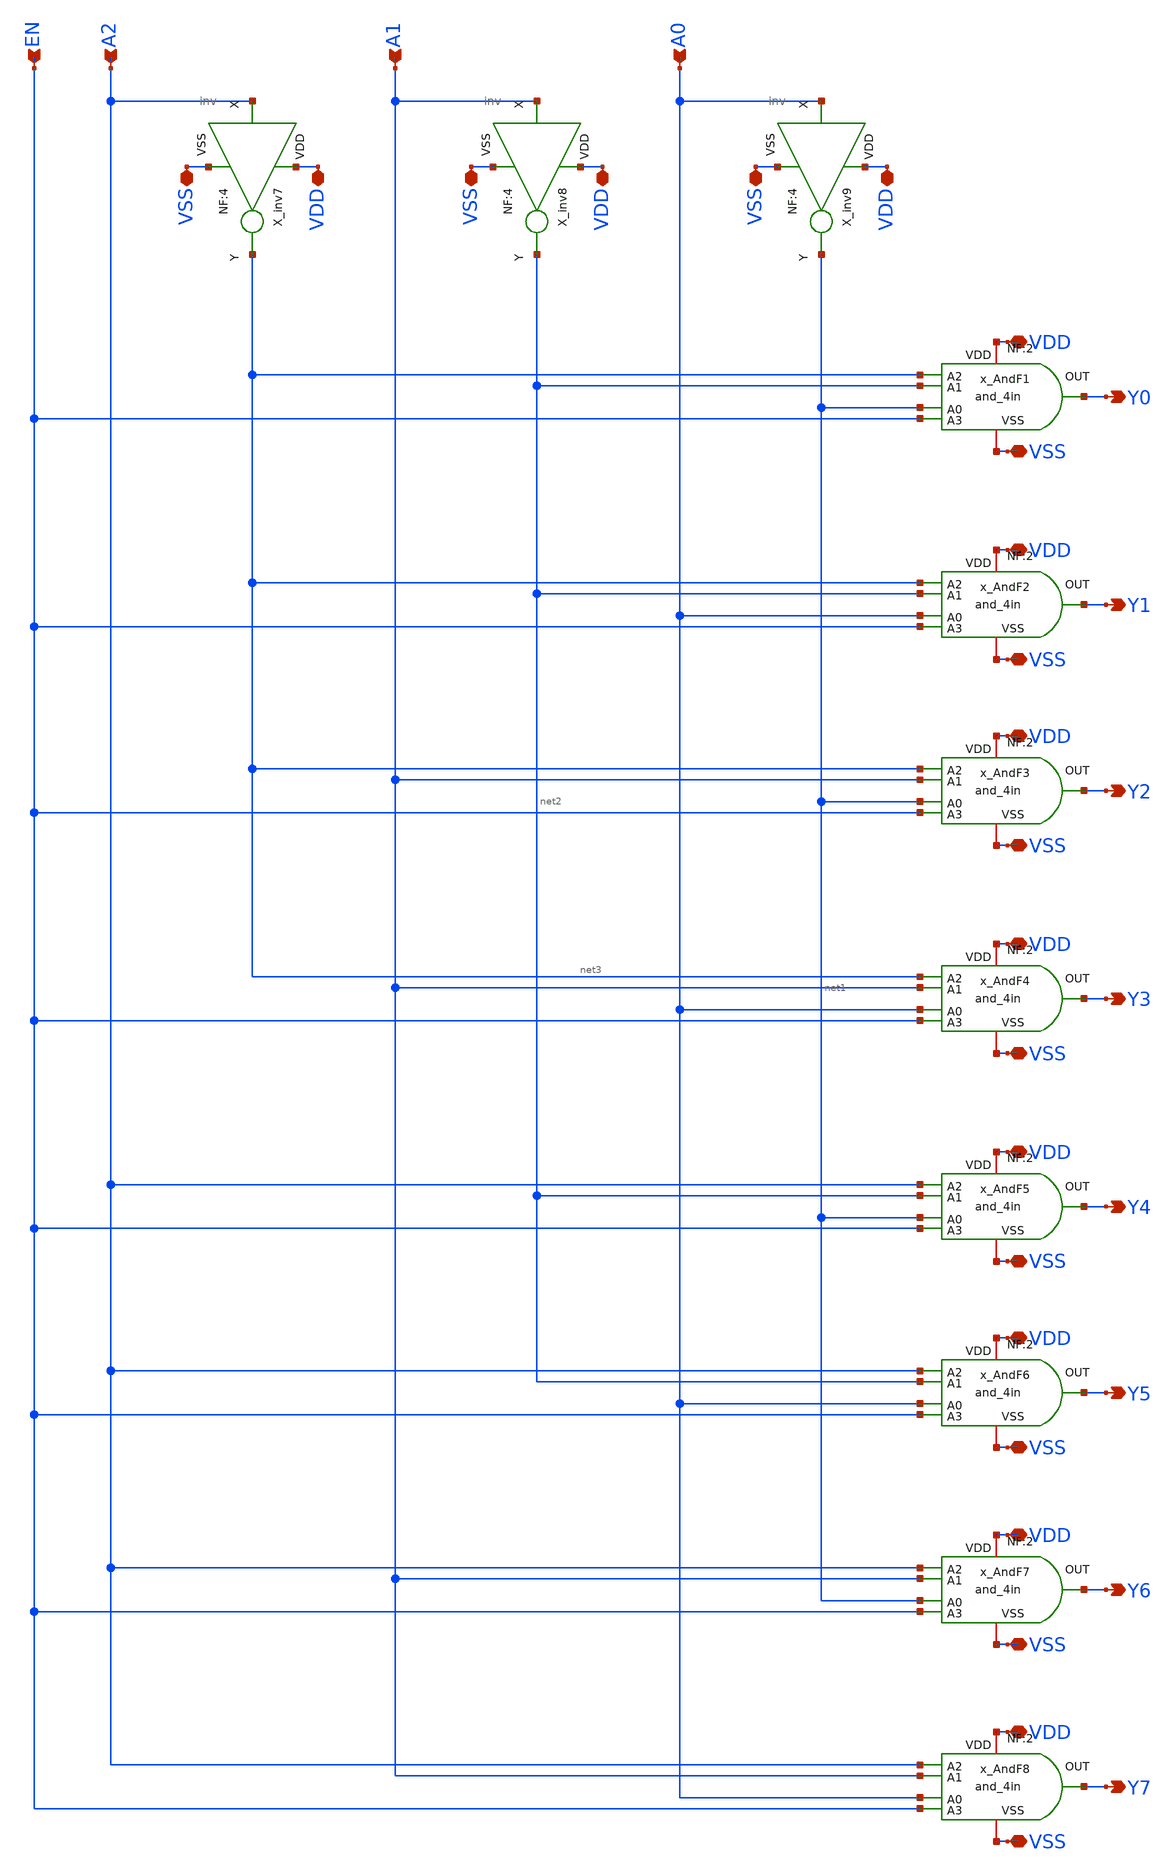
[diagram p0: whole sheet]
** sch_path: xschem_lib/dec_3to8_bak.sch
**.subckt dec_3to8_bak A2 A1 A0 VDD VDD VDD VDD VDD VDD VDD VDD VSS VSS VSS VSS VSS VSS VSS VSS VDD
*+ VDD VDD VSS VSS VSS Y0 Y1 Y2 Y3 Y4 Y5 Y6 Y7 EN
*.ipin A2
*.ipin A1
*.ipin A0
*.iopin VDD
*.iopin VDD
*.iopin VDD
*.iopin VDD
*.iopin VDD
*.iopin VDD
*.iopin VDD
*.iopin VDD
*.iopin VSS
*.iopin VSS
*.iopin VSS
*.iopin VSS
*.iopin VSS
*.iopin VSS
*.iopin VSS
*.iopin VSS
*.iopin VDD
*.iopin VDD
*.iopin VDD
*.iopin VSS
*.iopin VSS
*.iopin VSS
*.opin Y0
*.opin Y1
*.opin Y2
*.opin Y3
*.opin Y4
*.opin Y5
*.opin Y6
*.opin Y7
*.ipin EN
X_inv7 A2 VDD VSS net3 inv NF=4
X_inv8 A1 VDD VSS net2 inv NF=4
X_inv9 A0 VDD VSS net1 inv NF=4
x_AndF1 net3 net2 Y0 VDD VSS net1 EN and_4in NF=2
x_AndF2 net3 net2 Y1 VDD VSS A0 EN and_4in NF=2
x_AndF3 net3 A1 Y2 VDD VSS net1 EN and_4in NF=2
x_AndF4 net3 A1 Y3 VDD VSS A0 EN and_4in NF=2
x_AndF5 A2 net2 Y4 VDD VSS net1 EN and_4in NF=2
x_AndF6 A2 net2 Y5 VDD VSS A0 EN and_4in NF=2
x_AndF7 A2 A1 Y6 VDD VSS net1 EN and_4in NF=2
x_AndF8 A2 A1 Y7 VDD VSS A0 EN and_4in NF=2
**.ends
.end
